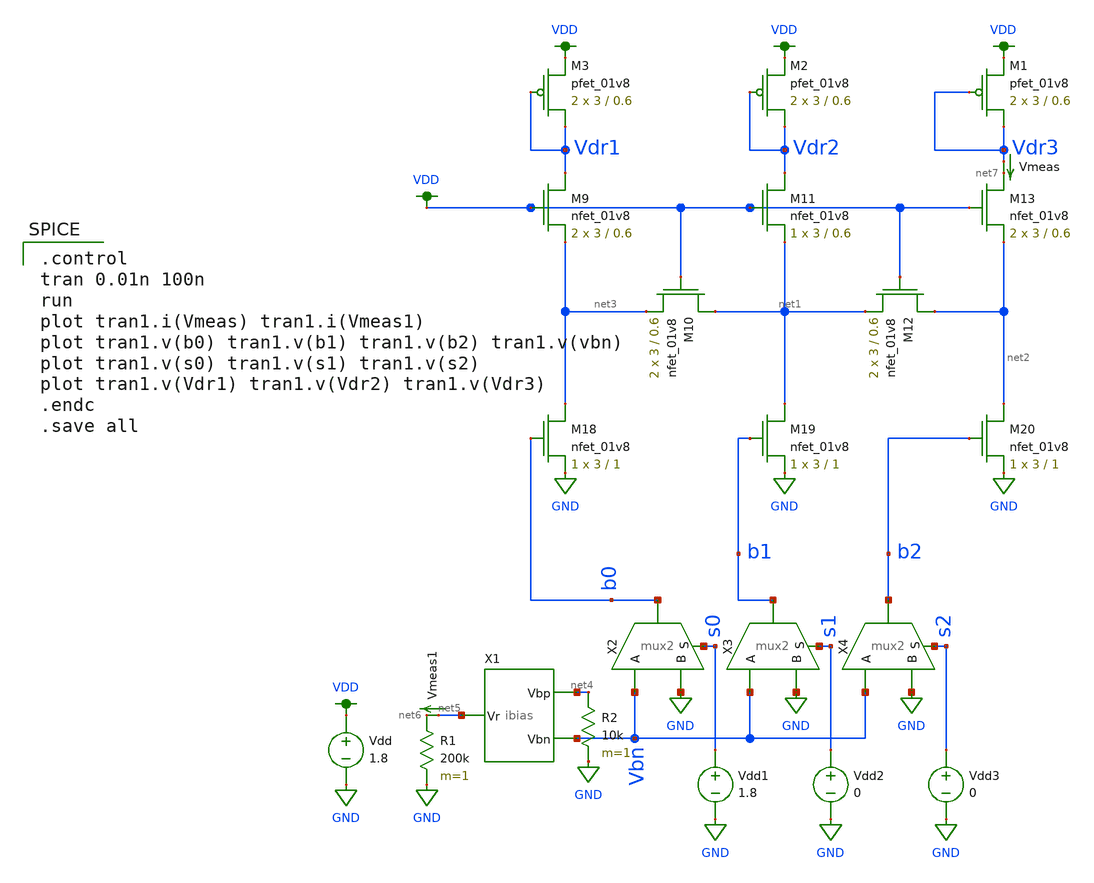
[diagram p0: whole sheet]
** sch_path: mini4/schem/ladder3_test.sch
**.subckt ladder3_test
X2 b0 Vbn GND s0 mux2
X3 b1 Vbn GND s1 mux2
X4 b2 Vbn GND s2 mux2
R1 net6 GND 200k m=1
Vdd VDD GND 1.8
Vdd1 s0 GND 1.8
Vdd2 s1 GND 0
Vdd3 s2 GND 0
XM9 Vdr1 VDD net3 GND sky130_fd_pr__nfet_01v8 L=0.6 W=3 nf=1 ad='int((nf+1)/2) * W/nf * 0.29' as='int((nf+2)/2) * W/nf * 0.29'
+ pd='2*int((nf+1)/2) * (W/nf + 0.29)' ps='2*int((nf+2)/2) * (W/nf + 0.29)' nrd='0.29 / W' nrs='0.29 / W'
+ sa=0 sb=0 sd=0 mult=2 m=2
XM10 net1 VDD net3 GND sky130_fd_pr__nfet_01v8 L=0.6 W=3 nf=1 ad='int((nf+1)/2) * W/nf * 0.29' as='int((nf+2)/2) * W/nf * 0.29'
+ pd='2*int((nf+1)/2) * (W/nf + 0.29)' ps='2*int((nf+2)/2) * (W/nf + 0.29)' nrd='0.29 / W' nrs='0.29 / W'
+ sa=0 sb=0 sd=0 mult=2 m=2
XM11 Vdr2 VDD net1 GND sky130_fd_pr__nfet_01v8 L=0.6 W=3 nf=1 ad='int((nf+1)/2) * W/nf * 0.29' as='int((nf+2)/2) * W/nf * 0.29'
+ pd='2*int((nf+1)/2) * (W/nf + 0.29)' ps='2*int((nf+2)/2) * (W/nf + 0.29)' nrd='0.29 / W' nrs='0.29 / W'
+ sa=0 sb=0 sd=0 mult=1 m=1
XM12 net2 VDD net1 GND sky130_fd_pr__nfet_01v8 L=0.6 W=3 nf=1 ad='int((nf+1)/2) * W/nf * 0.29' as='int((nf+2)/2) * W/nf * 0.29'
+ pd='2*int((nf+1)/2) * (W/nf + 0.29)' ps='2*int((nf+2)/2) * (W/nf + 0.29)' nrd='0.29 / W' nrs='0.29 / W'
+ sa=0 sb=0 sd=0 mult=2 m=2
XM13 net7 VDD net2 GND sky130_fd_pr__nfet_01v8 L=0.6 W=3 nf=1 ad='int((nf+1)/2) * W/nf * 0.29' as='int((nf+2)/2) * W/nf * 0.29'
+ pd='2*int((nf+1)/2) * (W/nf + 0.29)' ps='2*int((nf+2)/2) * (W/nf + 0.29)' nrd='0.29 / W' nrs='0.29 / W'
+ sa=0 sb=0 sd=0 mult=2 m=2
XM18 net3 b0 GND GND sky130_fd_pr__nfet_01v8 L=1 W=3 nf=1 ad='int((nf+1)/2) * W/nf * 0.29' as='int((nf+2)/2) * W/nf * 0.29'
+ pd='2*int((nf+1)/2) * (W/nf + 0.29)' ps='2*int((nf+2)/2) * (W/nf + 0.29)' nrd='0.29 / W' nrs='0.29 / W'
+ sa=0 sb=0 sd=0 mult=1 m=1
XM19 net1 b1 GND GND sky130_fd_pr__nfet_01v8 L=1 W=3 nf=1 ad='int((nf+1)/2) * W/nf * 0.29' as='int((nf+2)/2) * W/nf * 0.29'
+ pd='2*int((nf+1)/2) * (W/nf + 0.29)' ps='2*int((nf+2)/2) * (W/nf + 0.29)' nrd='0.29 / W' nrs='0.29 / W'
+ sa=0 sb=0 sd=0 mult=1 m=1
XM20 net2 b2 GND GND sky130_fd_pr__nfet_01v8 L=1 W=3 nf=1 ad='int((nf+1)/2) * W/nf * 0.29' as='int((nf+2)/2) * W/nf * 0.29'
+ pd='2*int((nf+1)/2) * (W/nf + 0.29)' ps='2*int((nf+2)/2) * (W/nf + 0.29)' nrd='0.29 / W' nrs='0.29 / W'
+ sa=0 sb=0 sd=0 mult=1 m=1
XM1 Vdr3 Vdr3 VDD VDD sky130_fd_pr__pfet_01v8 L=0.6 W=3 nf=1 ad='int((nf+1)/2) * W/nf * 0.29' as='int((nf+2)/2) * W/nf * 0.29'
+ pd='2*int((nf+1)/2) * (W/nf + 0.29)' ps='2*int((nf+2)/2) * (W/nf + 0.29)' nrd='0.29 / W' nrs='0.29 / W'
+ sa=0 sb=0 sd=0 mult=2 m=2
XM2 Vdr2 Vdr2 VDD VDD sky130_fd_pr__pfet_01v8 L=0.6 W=3 nf=1 ad='int((nf+1)/2) * W/nf * 0.29' as='int((nf+2)/2) * W/nf * 0.29'
+ pd='2*int((nf+1)/2) * (W/nf + 0.29)' ps='2*int((nf+2)/2) * (W/nf + 0.29)' nrd='0.29 / W' nrs='0.29 / W'
+ sa=0 sb=0 sd=0 mult=2 m=2
XM3 Vdr1 Vdr1 VDD VDD sky130_fd_pr__pfet_01v8 L=0.6 W=3 nf=1 ad='int((nf+1)/2) * W/nf * 0.29' as='int((nf+2)/2) * W/nf * 0.29'
+ pd='2*int((nf+1)/2) * (W/nf + 0.29)' ps='2*int((nf+2)/2) * (W/nf + 0.29)' nrd='0.29 / W' nrs='0.29 / W'
+ sa=0 sb=0 sd=0 mult=2 m=2
Vmeas Vdr3 net7 0
.save i(vmeas)
X1 net5 Vbn net4 ibias
R2 net4 GND 10k m=1
Vmeas1 net5 net6 0
.save i(vmeas1)
**** begin user architecture code

.option wnflag=1
.param MC_SWITCH=0.0
.lib ~/skywater/skywater-pdk/libraries/sky130_fd_pr_ngspice/latest/models/sky130.lib.spice tt


.control
tran 0.01n 100n
run
plot tran1.i(Vmeas) tran1.i(Vmeas1)
plot tran1.v(b0) tran1.v(b1) tran1.v(b2) tran1.v(vbn)
plot tran1.v(s0) tran1.v(s1) tran1.v(s2)
plot tran1.v(Vdr1) tran1.v(Vdr2) tran1.v(Vdr3)
.endc
.save all

**** end user architecture code
**.ends
.GLOBAL GND
.GLOBAL VDD
.end
